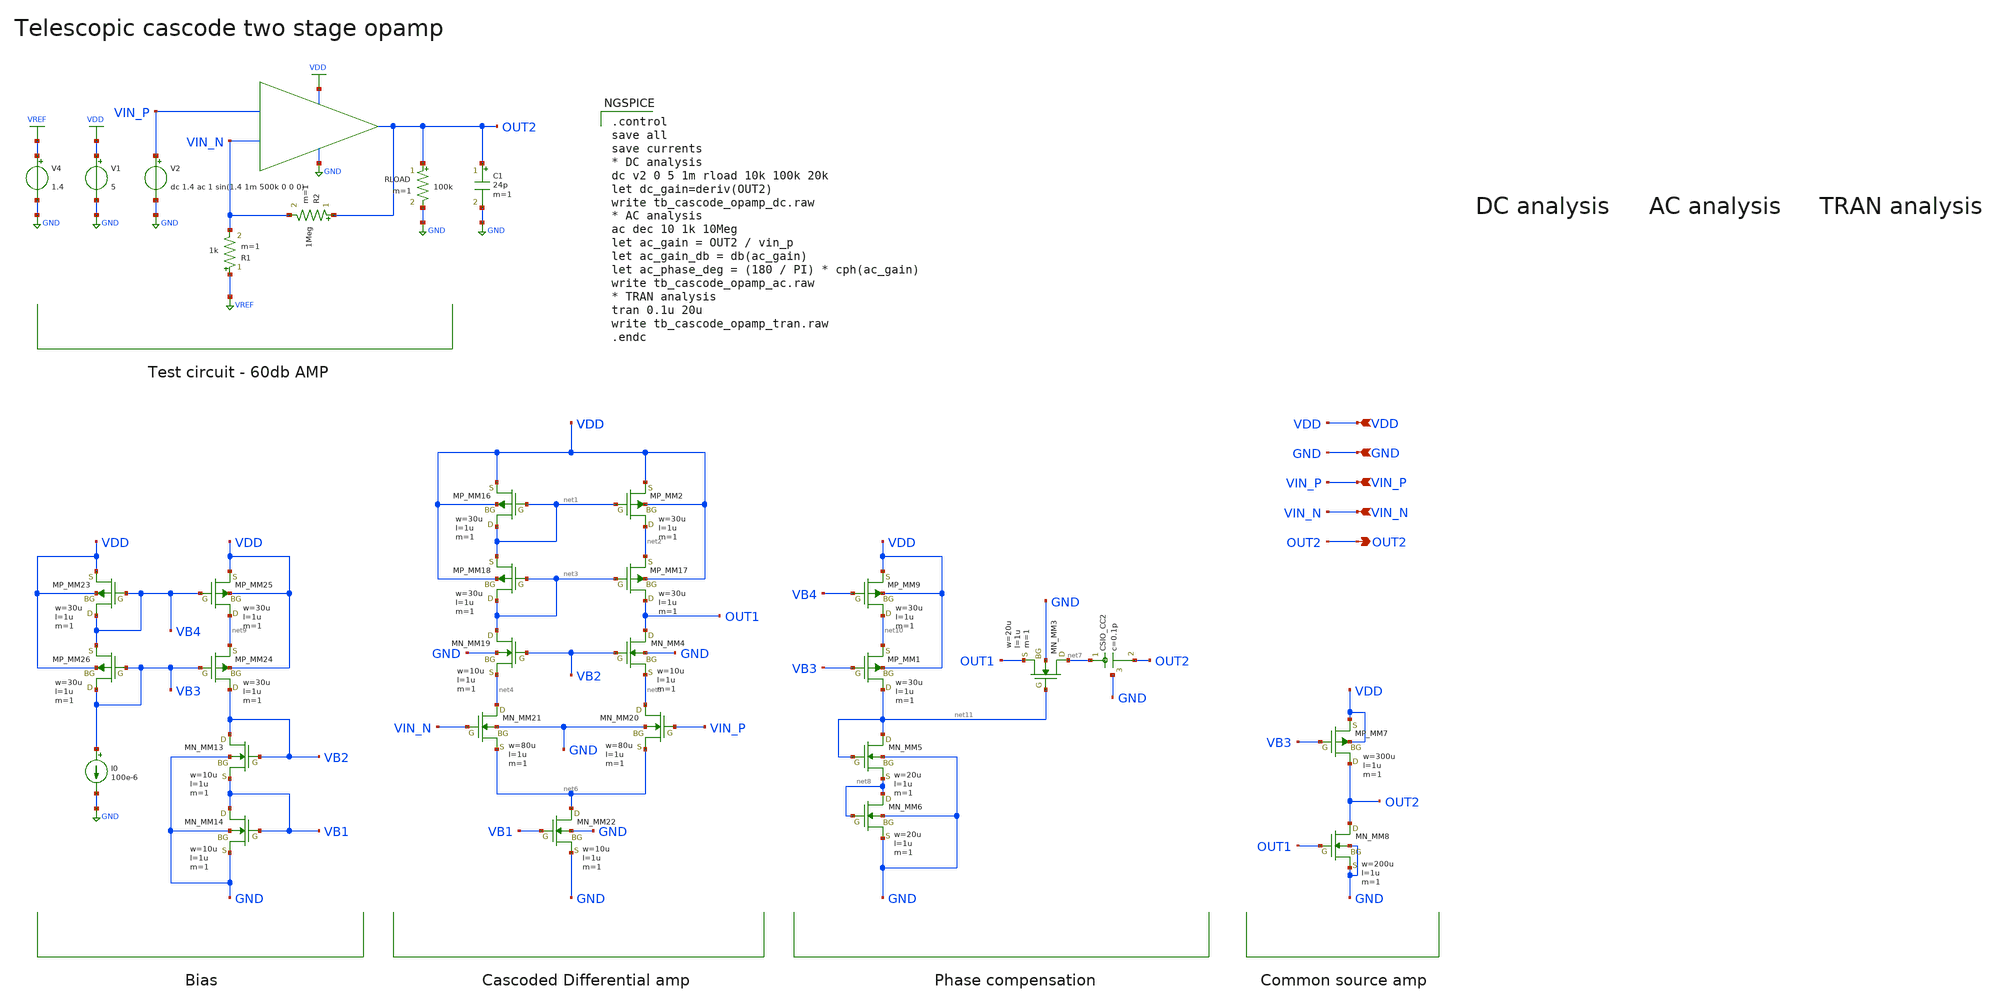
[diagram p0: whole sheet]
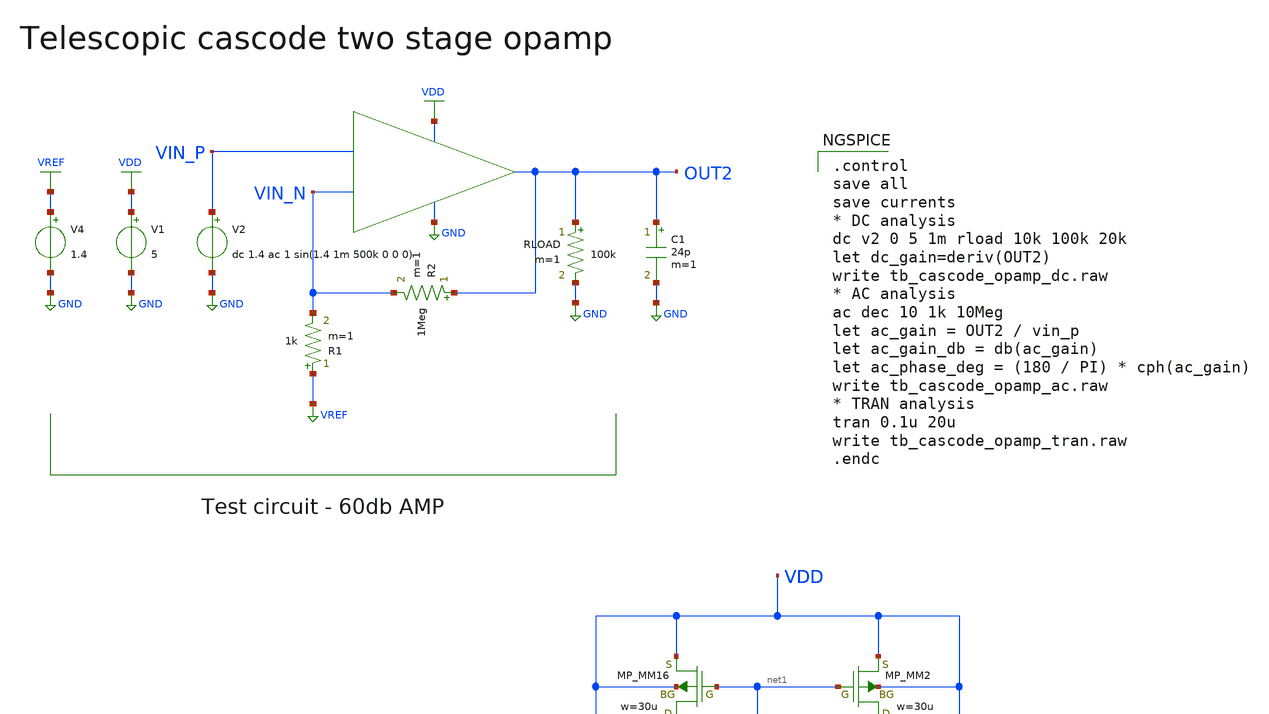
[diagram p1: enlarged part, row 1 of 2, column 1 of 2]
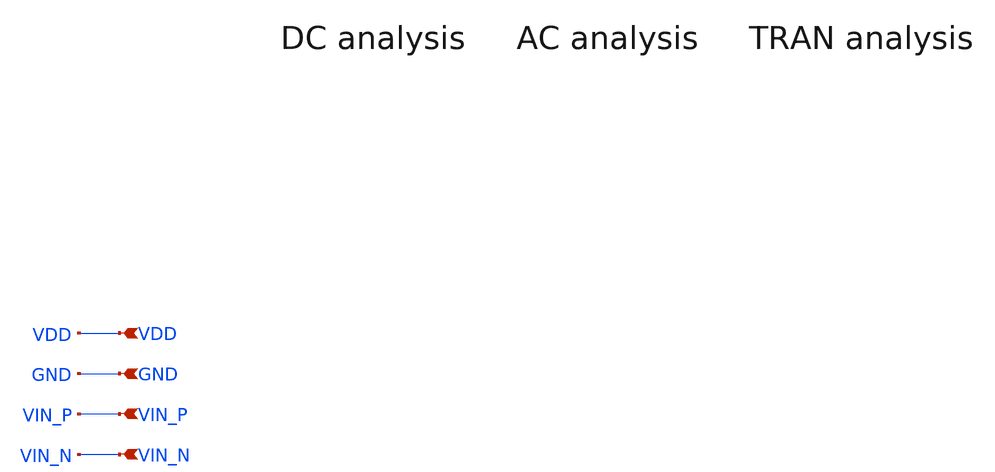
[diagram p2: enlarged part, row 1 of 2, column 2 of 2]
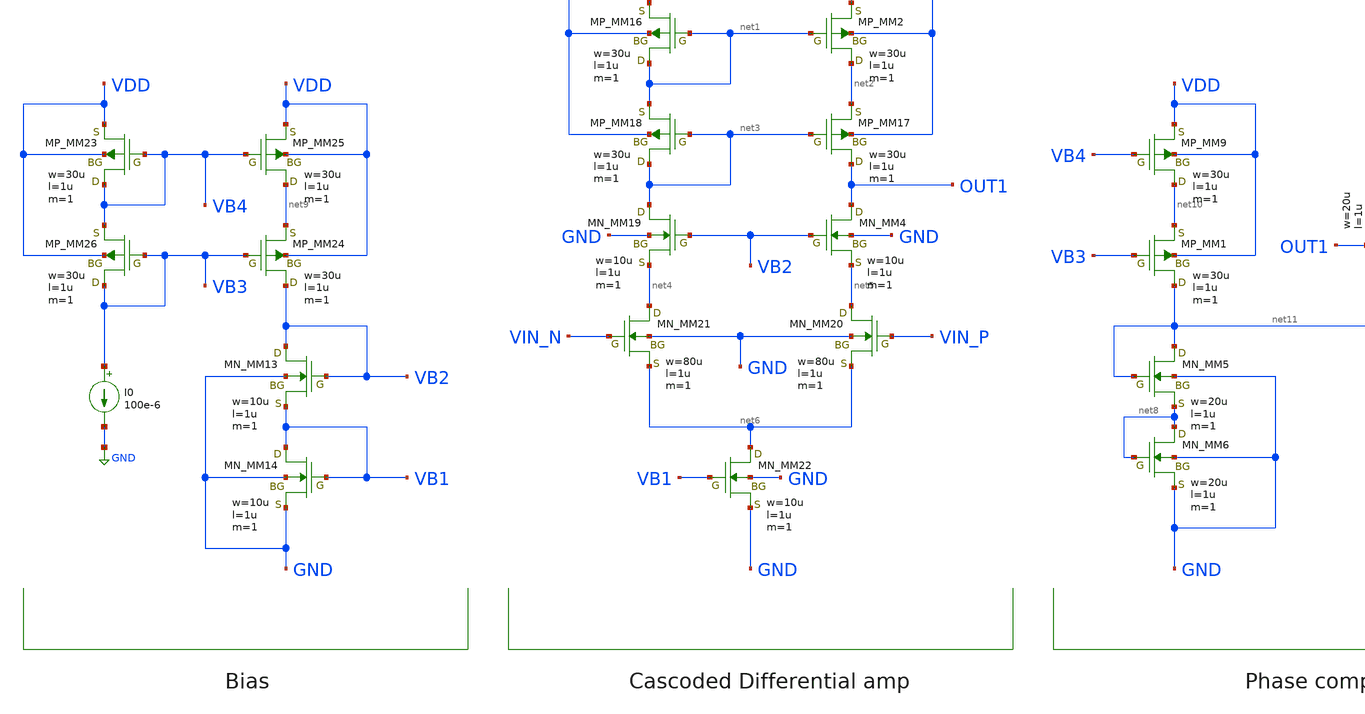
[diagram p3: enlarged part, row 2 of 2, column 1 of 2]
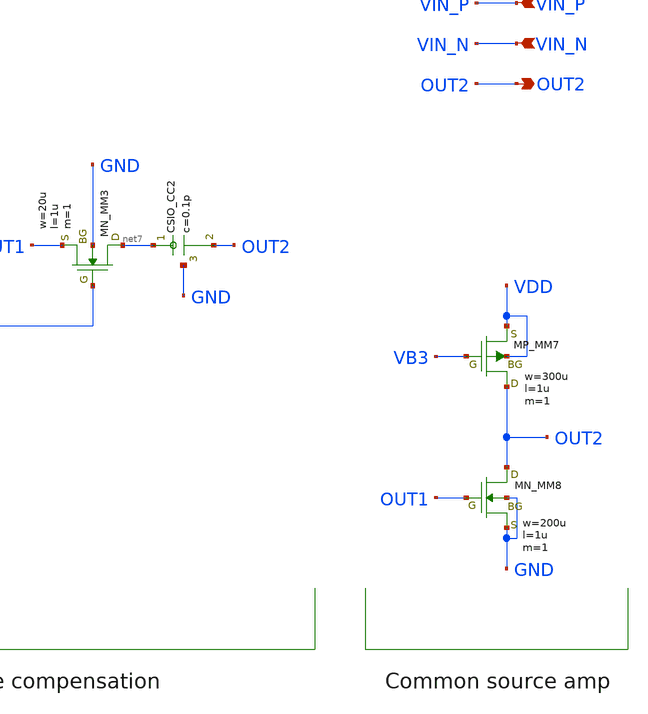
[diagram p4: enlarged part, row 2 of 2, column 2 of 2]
** sch_path: member_project/AM_Radio/Yamada3/xschem/tb_cascode_opamp.sch
**.subckt tb_cascode_opamp OUT2 VIN_N VIN_P GND VDD
*.opin OUT2
*.ipin VIN_N
*.ipin VIN_P
*.ipin GND
*.ipin VDD
I0 VB3 GND 100e-6
MM2 net2 net1 VDD VDD PMOS w=30u l=1u as=0 ad=0 ps=0 pd=0 nrd=0 nrs=0 m=1
MM4 OUT1 VB2 net5 GND NMOS w=10u l=1u as=0 ad=0 ps=0 pd=0 nrd=0 nrs=0 m=1
MM7 OUT2 VB3 VDD VDD PMOS w=300u l=1u as=0 ad=0 ps=0 pd=0 nrd=0 nrs=0 m=1
MM8 OUT2 OUT1 GND GND NMOS w=200u l=1u as=0 ad=0 ps=0 pd=0 nrd=0 nrs=0 m=1
MM16 net1 net1 VDD VDD PMOS w=30u l=1u as=0 ad=0 ps=0 pd=0 nrd=0 nrs=0 m=1
MM17 OUT1 net3 net2 VDD PMOS w=30u l=1u as=0 ad=0 ps=0 pd=0 nrd=0 nrs=0 m=1
MM18 net3 net3 net1 VDD PMOS w=30u l=1u as=0 ad=0 ps=0 pd=0 nrd=0 nrs=0 m=1
MM19 net3 VB2 net4 GND NMOS w=10u l=1u as=0 ad=0 ps=0 pd=0 nrd=0 nrs=0 m=1
MM20 net5 VIN_P net6 GND NMOS w=80u l=1u as=0 ad=0 ps=0 pd=0 nrd=0 nrs=0 m=1
MM21 net4 VIN_N net6 GND NMOS w=80u l=1u as=0 ad=0 ps=0 pd=0 nrd=0 nrs=0 m=1
MM22 net6 VB1 GND GND NMOS w=10u l=1u as=0 ad=0 ps=0 pd=0 nrd=0 nrs=0 m=1
MM3 net7 net11 OUT1 GND NMOS w=20u l=1u as=0 ad=0 ps=0 pd=0 nrd=0 nrs=0 m=1
CC2 net7 OUT2 GND F_CSIO c=0.1p x=120u y=120u m=1
MM5 net11 net11 net8 GND NMOS w=20u l=1u as=0 ad=0 ps=0 pd=0 nrd=0 nrs=0 m=1
MM6 net8 net8 GND GND NMOS w=20u l=1u as=0 ad=0 ps=0 pd=0 nrd=0 nrs=0 m=1
MM13 VB2 VB2 VB1 GND NMOS w=10u l=1u as=0 ad=0 ps=0 pd=0 nrd=0 nrs=0 m=1
MM14 VB1 VB1 GND GND NMOS w=10u l=1u as=0 ad=0 ps=0 pd=0 nrd=0 nrs=0 m=1
MM23 VB4 VB4 VDD VDD PMOS w=30u l=1u as=0 ad=0 ps=0 pd=0 nrd=0 nrs=0 m=1
MM24 VB2 VB3 net9 VDD PMOS w=30u l=1u as=0 ad=0 ps=0 pd=0 nrd=0 nrs=0 m=1
MM25 net9 VB4 VDD VDD PMOS w=30u l=1u as=0 ad=0 ps=0 pd=0 nrd=0 nrs=0 m=1
MM26 VB3 VB3 VB4 VDD PMOS w=30u l=1u as=0 ad=0 ps=0 pd=0 nrd=0 nrs=0 m=1
V1 VDD GND 5
R2 OUT2 VIN_N 1Meg m=1
V2 VIN_P GND dc 1.4 ac 1 sin(1.4 1m 500k 0 0 0)
V4 VREF GND 1.4
RLOAD OUT2 GND 100k m=1
MM1 net11 VB3 net10 VDD PMOS w=30u l=1u as=0 ad=0 ps=0 pd=0 nrd=0 nrs=0 m=1
MM9 net10 VB4 VDD VDD PMOS w=30u l=1u as=0 ad=0 ps=0 pd=0 nrd=0 nrs=0 m=1
C1 OUT2 GND 24p m=1
R1 VREF VIN_N 1k m=1
**** begin user architecture code
 .include $::LIB/ip62_models

.control
save all
save currents
* DC analysis
dc v2 0 5 1m rload 10k 100k 20k
let dc_gain=deriv(OUT2)
write tb_cascode_opamp_dc.raw
* AC analysis
ac dec 10 1k 10Meg
let ac_gain = OUT2 / vin_p
let ac_gain_db = db(ac_gain)
let ac_phase_deg = (180 / PI) * cph(ac_gain)
write tb_cascode_opamp_ac.raw
* TRAN analysis
tran 0.1u 20u
write tb_cascode_opamp_tran.raw
.endc


**** end user architecture code
**.ends
.GLOBAL VDD
.GLOBAL GND
.GLOBAL VREF
.end
